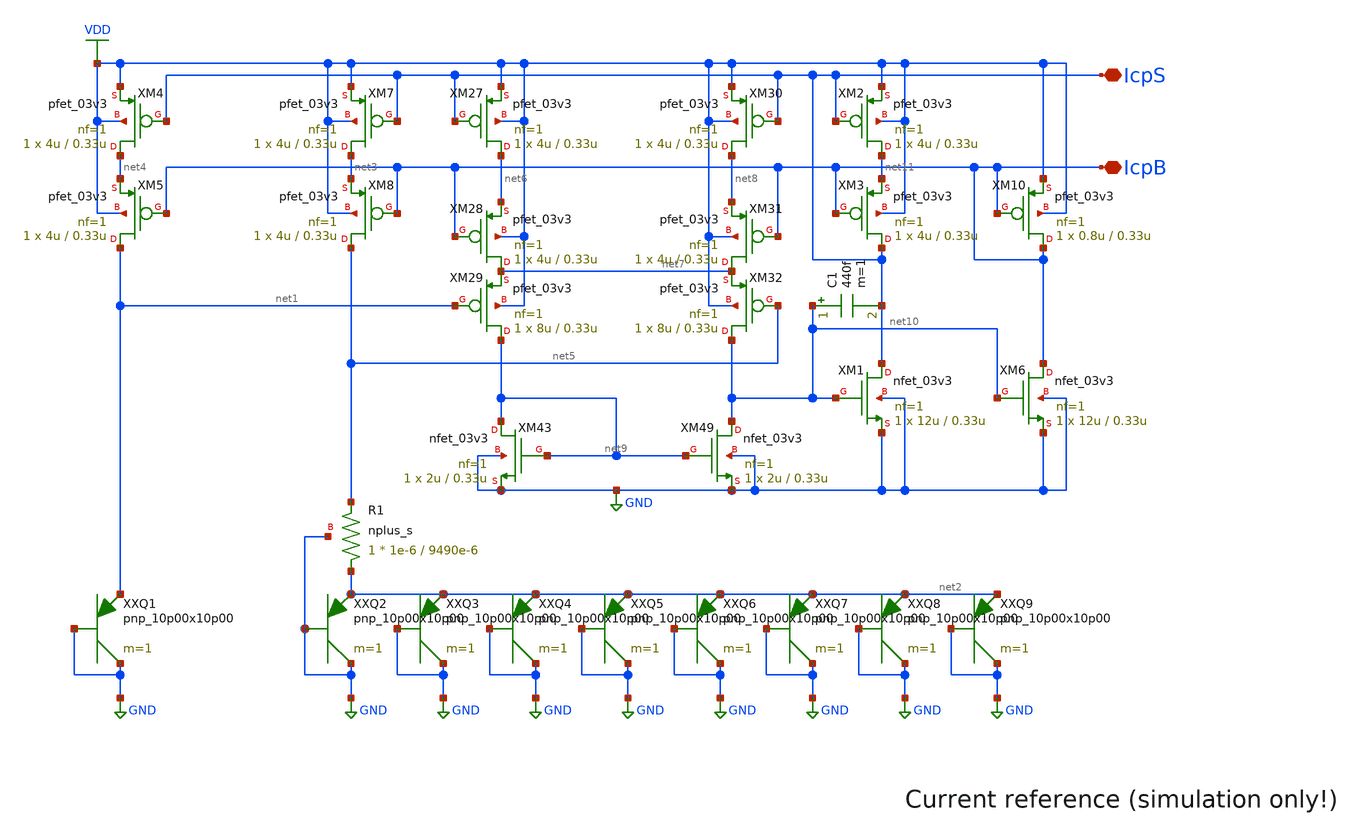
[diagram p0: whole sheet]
** sch_path: bgcs.sch
**.subckt bgcs IcpS IcpB
*.iopin IcpS
*.iopin IcpB
XXQ1 GND GND net1 pnp_10p00x10p00 m=1
XXQ2 GND GND net2 pnp_10p00x10p00 m=1
XR1 net2 net5 GND nplus_s r_width=1e-6 r_length=9490e-6 m=1
XXQ3 GND GND net2 pnp_10p00x10p00 m=1
XXQ4 GND GND net2 pnp_10p00x10p00 m=1
XXQ5 GND GND net2 pnp_10p00x10p00 m=1
XXQ6 GND GND net2 pnp_10p00x10p00 m=1
XXQ7 GND GND net2 pnp_10p00x10p00 m=1
XXQ8 GND GND net2 pnp_10p00x10p00 m=1
XXQ9 GND GND net2 pnp_10p00x10p00 m=1
XM7 net3 IcpS VDD VDD pfet_03v3 L=0.33u W=4u nf=1 ad='int((nf+1)/2) * W/nf * 0.18u' as='int((nf+2)/2) * W/nf * 0.18u'
+ pd='2*int((nf+1)/2) * (W/nf + 0.18u)' ps='2*int((nf+2)/2) * (W/nf + 0.18u)' nrd='0.18u / W' nrs='0.18u / W'
+ sa=0 sb=0 sd=0 m=1
XM8 net5 IcpB net3 VDD pfet_03v3 L=0.33u W=4u nf=1 ad='int((nf+1)/2) * W/nf * 0.18u' as='int((nf+2)/2) * W/nf * 0.18u'
+ pd='2*int((nf+1)/2) * (W/nf + 0.18u)' ps='2*int((nf+2)/2) * (W/nf + 0.18u)' nrd='0.18u / W' nrs='0.18u / W'
+ sa=0 sb=0 sd=0 m=1
XM4 net4 IcpS VDD VDD pfet_03v3 L=0.33u W=4u nf=1 ad='int((nf+1)/2) * W/nf * 0.18u' as='int((nf+2)/2) * W/nf * 0.18u'
+ pd='2*int((nf+1)/2) * (W/nf + 0.18u)' ps='2*int((nf+2)/2) * (W/nf + 0.18u)' nrd='0.18u / W' nrs='0.18u / W'
+ sa=0 sb=0 sd=0 m=1
XM5 net1 IcpB net4 VDD pfet_03v3 L=0.33u W=4u nf=1 ad='int((nf+1)/2) * W/nf * 0.18u' as='int((nf+2)/2) * W/nf * 0.18u'
+ pd='2*int((nf+1)/2) * (W/nf + 0.18u)' ps='2*int((nf+2)/2) * (W/nf + 0.18u)' nrd='0.18u / W' nrs='0.18u / W'
+ sa=0 sb=0 sd=0 m=1
XM29 net9 net1 net7 VDD pfet_03v3 L=0.33u W=8u nf=1 ad='int((nf+1)/2) * W/nf * 0.18u' as='int((nf+2)/2) * W/nf * 0.18u'
+ pd='2*int((nf+1)/2) * (W/nf + 0.18u)' ps='2*int((nf+2)/2) * (W/nf + 0.18u)' nrd='0.18u / W' nrs='0.18u / W'
+ sa=0 sb=0 sd=0 m=1
XM32 net10 net5 net7 VDD pfet_03v3 L=0.33u W=8u nf=1 ad='int((nf+1)/2) * W/nf * 0.18u' as='int((nf+2)/2) * W/nf * 0.18u'
+ pd='2*int((nf+1)/2) * (W/nf + 0.18u)' ps='2*int((nf+2)/2) * (W/nf + 0.18u)' nrd='0.18u / W' nrs='0.18u / W'
+ sa=0 sb=0 sd=0 m=1
XM27 net6 IcpS VDD VDD pfet_03v3 L=0.33u W=4u nf=1 ad='int((nf+1)/2) * W/nf * 0.18u' as='int((nf+2)/2) * W/nf * 0.18u'
+ pd='2*int((nf+1)/2) * (W/nf + 0.18u)' ps='2*int((nf+2)/2) * (W/nf + 0.18u)' nrd='0.18u / W' nrs='0.18u / W'
+ sa=0 sb=0 sd=0 m=1
XM28 net7 IcpB net6 VDD pfet_03v3 L=0.33u W=4u nf=1 ad='int((nf+1)/2) * W/nf * 0.18u' as='int((nf+2)/2) * W/nf * 0.18u'
+ pd='2*int((nf+1)/2) * (W/nf + 0.18u)' ps='2*int((nf+2)/2) * (W/nf + 0.18u)' nrd='0.18u / W' nrs='0.18u / W'
+ sa=0 sb=0 sd=0 m=1
XM30 net8 IcpS VDD VDD pfet_03v3 L=0.33u W=4u nf=1 ad='int((nf+1)/2) * W/nf * 0.18u' as='int((nf+2)/2) * W/nf * 0.18u'
+ pd='2*int((nf+1)/2) * (W/nf + 0.18u)' ps='2*int((nf+2)/2) * (W/nf + 0.18u)' nrd='0.18u / W' nrs='0.18u / W'
+ sa=0 sb=0 sd=0 m=1
XM31 net7 IcpB net8 VDD pfet_03v3 L=0.33u W=4u nf=1 ad='int((nf+1)/2) * W/nf * 0.18u' as='int((nf+2)/2) * W/nf * 0.18u'
+ pd='2*int((nf+1)/2) * (W/nf + 0.18u)' ps='2*int((nf+2)/2) * (W/nf + 0.18u)' nrd='0.18u / W' nrs='0.18u / W'
+ sa=0 sb=0 sd=0 m=1
XM43 net9 net9 GND GND nfet_03v3 L=0.33u W=2u nf=1 ad='int((nf+1)/2) * W/nf * 0.18u' as='int((nf+2)/2) * W/nf * 0.18u'
+ pd='2*int((nf+1)/2) * (W/nf + 0.18u)' ps='2*int((nf+2)/2) * (W/nf + 0.18u)' nrd='0.18u / W' nrs='0.18u / W'
+ sa=0 sb=0 sd=0 m=1
XM49 net10 net9 GND GND nfet_03v3 L=0.33u W=2u nf=1 ad='int((nf+1)/2) * W/nf * 0.18u' as='int((nf+2)/2) * W/nf * 0.18u'
+ pd='2*int((nf+1)/2) * (W/nf + 0.18u)' ps='2*int((nf+2)/2) * (W/nf + 0.18u)' nrd='0.18u / W' nrs='0.18u / W'
+ sa=0 sb=0 sd=0 m=1
XM1 IcpS net10 GND GND nfet_03v3 L=0.33u W=12u nf=1 ad='int((nf+1)/2) * W/nf * 0.18u' as='int((nf+2)/2) * W/nf * 0.18u'
+ pd='2*int((nf+1)/2) * (W/nf + 0.18u)' ps='2*int((nf+2)/2) * (W/nf + 0.18u)' nrd='0.18u / W' nrs='0.18u / W'
+ sa=0 sb=0 sd=0 m=1
XM2 net11 IcpS VDD VDD pfet_03v3 L=0.33u W=4u nf=1 ad='int((nf+1)/2) * W/nf * 0.18u' as='int((nf+2)/2) * W/nf * 0.18u'
+ pd='2*int((nf+1)/2) * (W/nf + 0.18u)' ps='2*int((nf+2)/2) * (W/nf + 0.18u)' nrd='0.18u / W' nrs='0.18u / W'
+ sa=0 sb=0 sd=0 m=1
XM3 IcpS IcpB net11 VDD pfet_03v3 L=0.33u W=4u nf=1 ad='int((nf+1)/2) * W/nf * 0.18u' as='int((nf+2)/2) * W/nf * 0.18u'
+ pd='2*int((nf+1)/2) * (W/nf + 0.18u)' ps='2*int((nf+2)/2) * (W/nf + 0.18u)' nrd='0.18u / W' nrs='0.18u / W'
+ sa=0 sb=0 sd=0 m=1
XM6 IcpB net10 GND GND nfet_03v3 L=0.33u W=12u nf=1 ad='int((nf+1)/2) * W/nf * 0.18u' as='int((nf+2)/2) * W/nf * 0.18u'
+ pd='2*int((nf+1)/2) * (W/nf + 0.18u)' ps='2*int((nf+2)/2) * (W/nf + 0.18u)' nrd='0.18u / W' nrs='0.18u / W'
+ sa=0 sb=0 sd=0 m=1
XM10 IcpB IcpB VDD VDD pfet_03v3 L=0.33u W=0.8u nf=1 ad='int((nf+1)/2) * W/nf * 0.18u' as='int((nf+2)/2) * W/nf * 0.18u'
+ pd='2*int((nf+1)/2) * (W/nf + 0.18u)' ps='2*int((nf+2)/2) * (W/nf + 0.18u)' nrd='0.18u / W' nrs='0.18u / W'
+ sa=0 sb=0 sd=0 m=1
C1 net10 IcpS 440f m=1
**.ends
.GLOBAL GND
.GLOBAL VDD
.end
